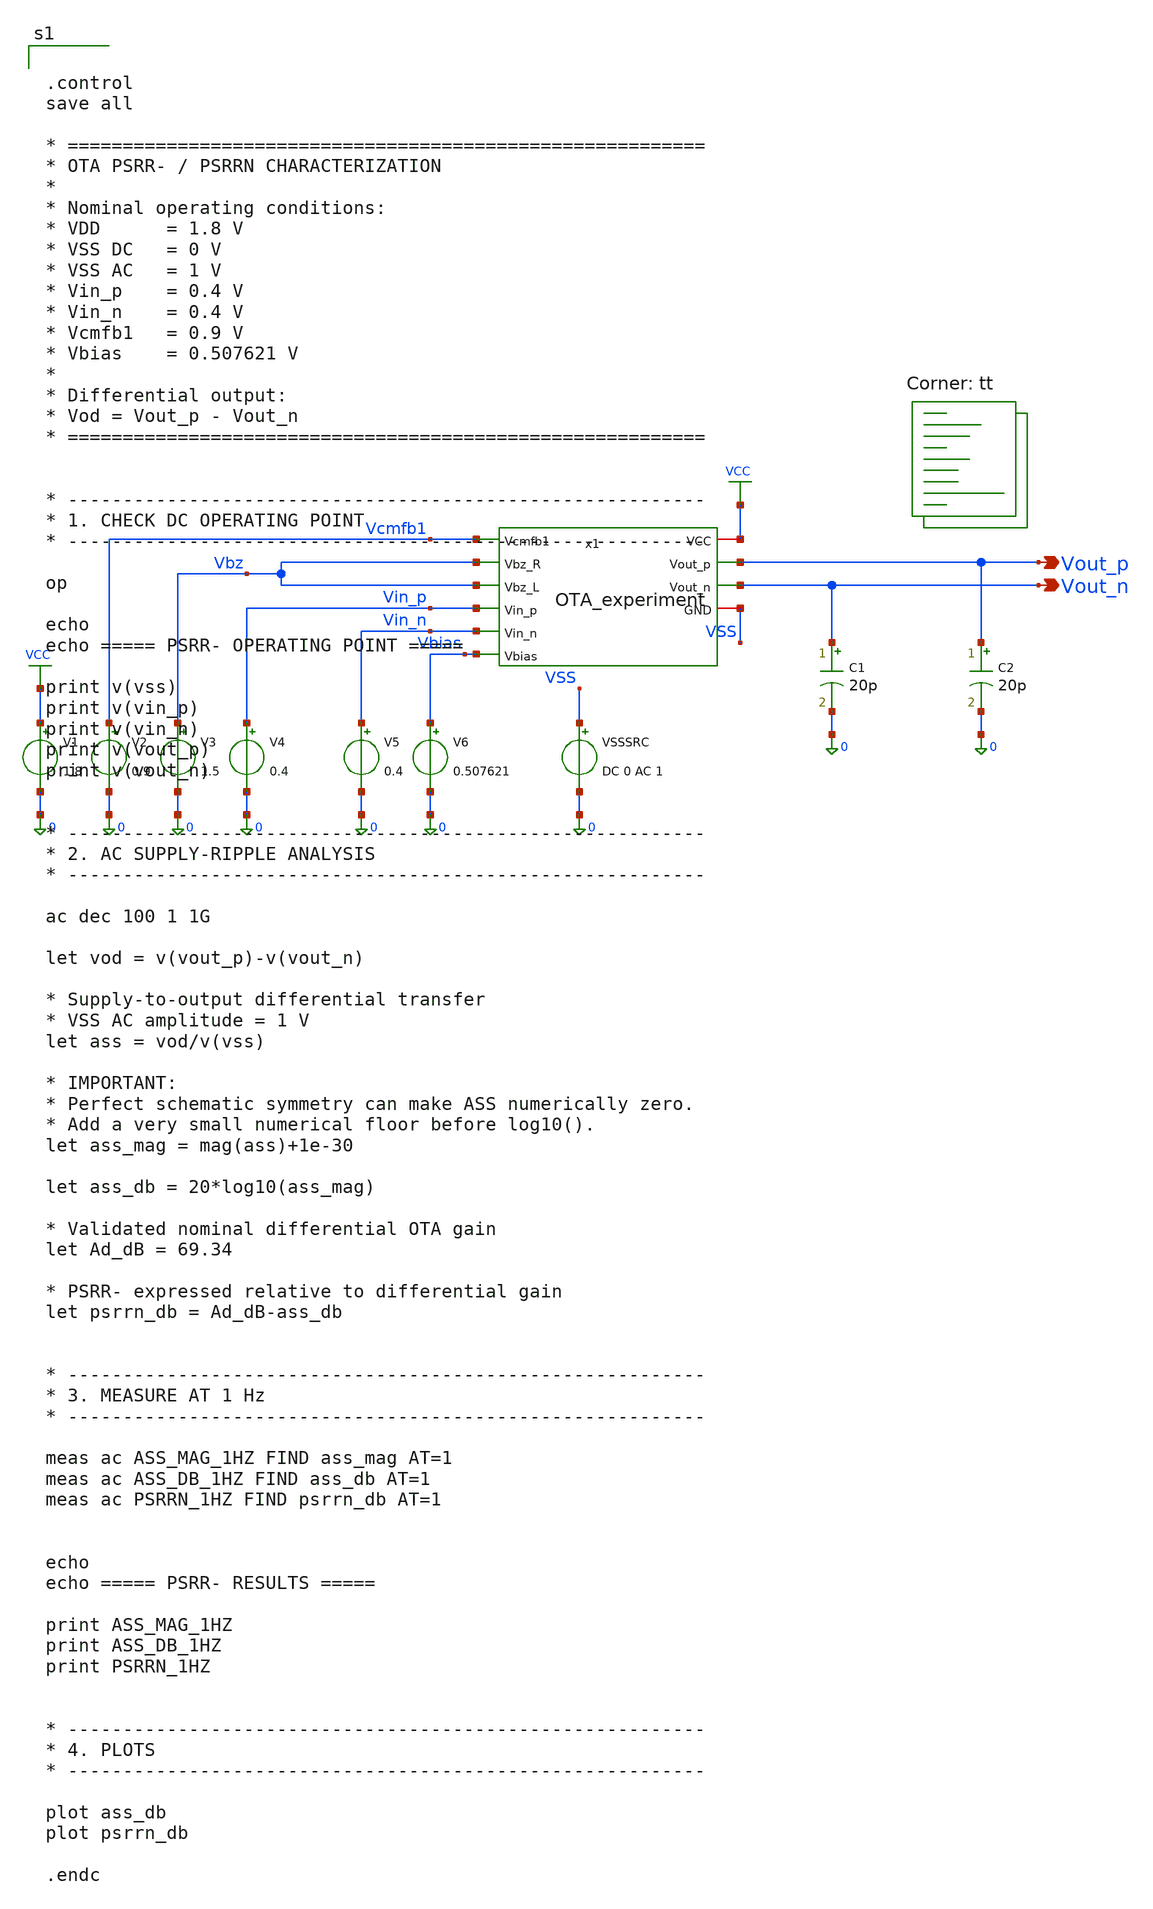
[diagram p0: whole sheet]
** sch_path: blocks/01_OTA/sim/tb_OTA_PSRRN_experiment.sch
**.subckt tb_OTA_PSRRN_experiment Vout_p Vout_n
*.opin Vout_p
*.opin Vout_n
V1 VCC 0 1.8
V2 Vcmfb1 0 0.9
V3 Vbz 0 1.5
V4 Vin_p 0 0.4
V5 Vin_n 0 0.4
V6 Vbias 0 0.507621
VSSSRC VSS 0 DC 0 AC 1
C1 Vout_n 0 20p m=1
C2 Vout_p 0 20p m=1
x1 VCC Vcmfb1 Vbz Vbz Vin_p Vin_n Vout_p Vout_n Vbias VSS OTA_experiment
**** begin user architecture code


.control
save all

* ==========================================================
* OTA PSRR- / PSRRN CHARACTERIZATION
*
* Nominal operating conditions:
* VDD      = 1.8 V
* VSS DC   = 0 V
* VSS AC   = 1 V
* Vin_p    = 0.4 V
* Vin_n    = 0.4 V
* Vcmfb1   = 0.9 V
* Vbias    = 0.507621 V
*
* Differential output:
* Vod = Vout_p - Vout_n
* ==========================================================


* ----------------------------------------------------------
* 1. CHECK DC OPERATING POINT
* ----------------------------------------------------------

op

echo
echo ===== PSRR- OPERATING POINT =====

print v(vss)
print v(vin_p)
print v(vin_n)
print v(vout_p)
print v(vout_n)


* ----------------------------------------------------------
* 2. AC SUPPLY-RIPPLE ANALYSIS
* ----------------------------------------------------------

ac dec 100 1 1G

let vod = v(vout_p)-v(vout_n)

* Supply-to-output differential transfer
* VSS AC amplitude = 1 V
let ass = vod/v(vss)

* IMPORTANT:
* Perfect schematic symmetry can make ASS numerically zero.
* Add a very small numerical floor before log10().
let ass_mag = mag(ass)+1e-30

let ass_db = 20*log10(ass_mag)

* Validated nominal differential OTA gain
let Ad_dB = 69.34

* PSRR- expressed relative to differential gain
let psrrn_db = Ad_dB-ass_db


* ----------------------------------------------------------
* 3. MEASURE AT 1 Hz
* ----------------------------------------------------------

meas ac ASS_MAG_1HZ FIND ass_mag AT=1
meas ac ASS_DB_1HZ FIND ass_db AT=1
meas ac PSRRN_1HZ FIND psrrn_db AT=1


echo
echo ===== PSRR- RESULTS =====

print ASS_MAG_1HZ
print ASS_DB_1HZ
print PSRRN_1HZ


* ----------------------------------------------------------
* 4. PLOTS
* ----------------------------------------------------------

plot ass_db
plot psrrn_db

.endc


.lib $::SKYWATER_MODELS/sky130.lib.spice tt
**** end user architecture code
**.ends

* expanding   symbol:  blocks/01_OTA/xschem/OTA_experiment.sym # of pins=10
** sym_path: blocks/01_OTA/xschem/OTA_experiment.sym
** sch_path: blocks/01_OTA/xschem/OTA_experiment.sch
.subckt OTA_experiment VCC Vcmfb1 Vbz_R Vbz_L Vin_p Vin_n Vout_p Vout_n Vbias GND
*.ipin Vin_p
*.ipin Vin_n
*.ipin Vbias
*.ipin Vbz_R
*.ipin Vbz_L
*.ipin Vcmfb1
*.opin Vout_p
*.opin Vout_n
*.iopin VCC
*.iopin GND
XM1 net5 Vin_p net3 net5 sky130_fd_pr__pfet_01v8 L=1.2 W=120 nf=1 ad='int((1 + 1)/2) * 120 / 1 * 0.29'
+ as='int((1 + 2)/2) * 120 / 1 * 0.29' pd='2*int((1 + 1)/2) * (120 / 1 + 0.29)' ps='2*int((1 + 2)/2) * (120 / 1 + 0.29)'
+ nrd='0.29 / 120 ' nrs='0.29 / 120 ' sa=0 sb=0 sd=0 mult=1 m=1
XM2 net5 Vin_n net4 net5 sky130_fd_pr__pfet_01v8 L=1.2 W=120 nf=1 ad='int((1 + 1)/2) * 120 / 1 * 0.29'
+ as='int((1 + 2)/2) * 120 / 1 * 0.29' pd='2*int((1 + 1)/2) * (120 / 1 + 0.29)' ps='2*int((1 + 2)/2) * (120 / 1 + 0.29)'
+ nrd='0.29 / 120 ' nrs='0.29 / 120 ' sa=0 sb=0 sd=0 mult=1 m=1
XM3 net3 Vbias GND GND sky130_fd_pr__nfet_01v8 L=2 W=8 nf=1 ad='int((1 + 1)/2) * 8 / 1 * 0.29' as='int((1 + 2)/2) * 8 / 1 * 0.29'
+ pd='2*int((1 + 1)/2) * (8 / 1 + 0.29)' ps='2*int((1 + 2)/2) * (8 / 1 + 0.29)' nrd='0.29 / 8 ' nrs='0.29 / 8 '
+ sa=0 sb=0 sd=0 mult=1 m=1
XM4 net4 Vbias GND GND sky130_fd_pr__nfet_01v8 L=2 W=8 nf=1 ad='int((1 + 1)/2) * 8 / 1 * 0.29' as='int((1 + 2)/2) * 8 / 1 * 0.29'
+ pd='2*int((1 + 1)/2) * (8 / 1 + 0.29)' ps='2*int((1 + 2)/2) * (8 / 1 + 0.29)' nrd='0.29 / 8 ' nrs='0.29 / 8 '
+ sa=0 sb=0 sd=0 mult=1 m=1
XM5 net1 net4 GND GND sky130_fd_pr__nfet_01v8 L=2 W=20 nf=1 ad='int((1 + 1)/2) * 20 / 1 * 0.29' as='int((1 + 2)/2) * 20 / 1 * 0.29'
+ pd='2*int((1 + 1)/2) * (20 / 1 + 0.29)' ps='2*int((1 + 2)/2) * (20 / 1 + 0.29)' nrd='0.29 / 20 ' nrs='0.29 / 20 '
+ sa=0 sb=0 sd=0 mult=1 m=1
XM6 net2 net3 GND GND sky130_fd_pr__nfet_01v8 L=2 W=20 nf=1 ad='int((1 + 1)/2) * 20 / 1 * 0.29' as='int((1 + 2)/2) * 20 / 1 * 0.29'
+ pd='2*int((1 + 1)/2) * (20 / 1 + 0.29)' ps='2*int((1 + 2)/2) * (20 / 1 + 0.29)' nrd='0.29 / 20 ' nrs='0.29 / 20 '
+ sa=0 sb=0 sd=0 mult=1 m=1
XM7 VCC net1 net1 VCC sky130_fd_pr__pfet_01v8 L=2 W=30 nf=1 ad='int((1 + 1)/2) * 30 / 1 * 0.29' as='int((1 + 2)/2) * 30 / 1 * 0.29'
+ pd='2*int((1 + 1)/2) * (30 / 1 + 0.29)' ps='2*int((1 + 2)/2) * (30 / 1 + 0.29)' nrd='0.29 / 30 ' nrs='0.29 / 30 '
+ sa=0 sb=0 sd=0 mult=1 m=1
XM8 VCC net2 net2 VCC sky130_fd_pr__pfet_01v8 L=2 W=30 nf=1 ad='int((1 + 1)/2) * 30 / 1 * 0.29' as='int((1 + 2)/2) * 30 / 1 * 0.29'
+ pd='2*int((1 + 1)/2) * (30 / 1 + 0.29)' ps='2*int((1 + 2)/2) * (30 / 1 + 0.29)' nrd='0.29 / 30 ' nrs='0.29 / 30 '
+ sa=0 sb=0 sd=0 mult=1 m=1
XM9 VCC net1 Vout_p VCC sky130_fd_pr__pfet_01v8 L=1 W=300 nf=1 ad='int((1 + 1)/2) * 300 / 1 * 0.29' as='int((1 + 2)/2) * 300 / 1 * 0.29'
+ pd='2*int((1 + 1)/2) * (300 / 1 + 0.29)' ps='2*int((1 + 2)/2) * (300 / 1 + 0.29)' nrd='0.29 / 300 ' nrs='0.29 / 300 '
+ sa=0 sb=0 sd=0 mult=1 m=1
XM10 VCC net2 Vout_n VCC sky130_fd_pr__pfet_01v8 L=1 W=300 nf=1 ad='int((1 + 1)/2) * 300 / 1 * 0.29'
+ as='int((1 + 2)/2) * 300 / 1 * 0.29' pd='2*int((1 + 1)/2) * (300 / 1 + 0.29)' ps='2*int((1 + 2)/2) * (300 / 1 + 0.29)'
+ nrd='0.29 / 300 ' nrs='0.29 / 300 ' sa=0 sb=0 sd=0 mult=1 m=1
XM11 Vout_p net4 GND GND sky130_fd_pr__nfet_01v8 L=1 W=200 nf=1 ad='int((1 + 1)/2) * 200 / 1 * 0.29'
+ as='int((1 + 2)/2) * 200 / 1 * 0.29' pd='2*int((1 + 1)/2) * (200 / 1 + 0.29)' ps='2*int((1 + 2)/2) * (200 / 1 + 0.29)'
+ nrd='0.29 / 200 ' nrs='0.29 / 200 ' sa=0 sb=0 sd=0 mult=1 m=1
XM12 Vout_n net3 GND GND sky130_fd_pr__nfet_01v8 L=1 W=200 nf=1 ad='int((1 + 1)/2) * 200 / 1 * 0.29'
+ as='int((1 + 2)/2) * 200 / 1 * 0.29' pd='2*int((1 + 1)/2) * (200 / 1 + 0.29)' ps='2*int((1 + 2)/2) * (200 / 1 + 0.29)'
+ nrd='0.29 / 200 ' nrs='0.29 / 200 ' sa=0 sb=0 sd=0 mult=1 m=1
XM13 VCC Vcmfb1 net5 VCC sky130_fd_pr__pfet_01v8 L=1.2 W=60 nf=1 ad='int((1 + 1)/2) * 60 / 1 * 0.29'
+ as='int((1 + 2)/2) * 60 / 1 * 0.29' pd='2*int((1 + 1)/2) * (60 / 1 + 0.29)' ps='2*int((1 + 2)/2) * (60 / 1 + 0.29)'
+ nrd='0.29 / 60 ' nrs='0.29 / 60 ' sa=0 sb=0 sd=0 mult=1 m=1
XC1 Vout_p net4 sky130_fd_pr__cap_mim_m3_1 W=1 L=1 MF=80 m=80
XC2 net3 Vout_n sky130_fd_pr__cap_mim_m3_1 W=1 L=1 MF=80 m=80
.ends

.GLOBAL VCC
.end
